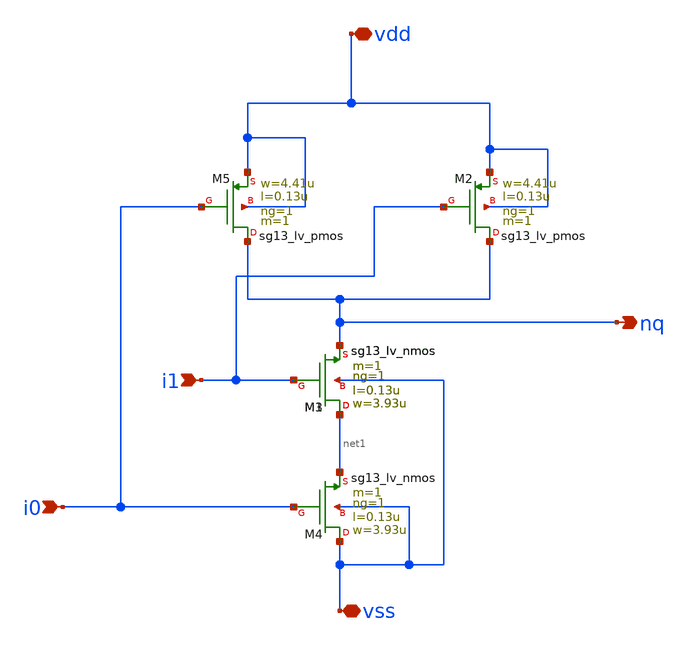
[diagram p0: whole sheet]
** sch_path: ihp-sg13g2/libs.ref/sg13g2_io/xschem/sg13g2_io_nand2_x1.sch
**.subckt sg13g2_io_nand2_x1 vdd vss i0 i1 nq
*.iopin vdd
*.iopin vss
*.ipin i0
*.ipin i1
*.opin nq
XM1 net1 i1 nq vss sg13_lv_nmos w=3.93u l=0.13u ng=1 m=1 mm_ok=1
XM2 nq i1 vdd vdd sg13_lv_pmos w=4.41u l=0.13u ng=1 m=1 mm_ok=1
XM3 net1 i1 nq vss sg13_lv_nmos w=3.93u l=0.13u ng=1 m=1 mm_ok=1
XM4 vss i0 net1 vss sg13_lv_nmos w=3.93u l=0.13u ng=1 m=1 mm_ok=1
XM5 nq i0 vdd vdd sg13_lv_pmos w=4.41u l=0.13u ng=1 m=1 mm_ok=1
**.ends
.end
